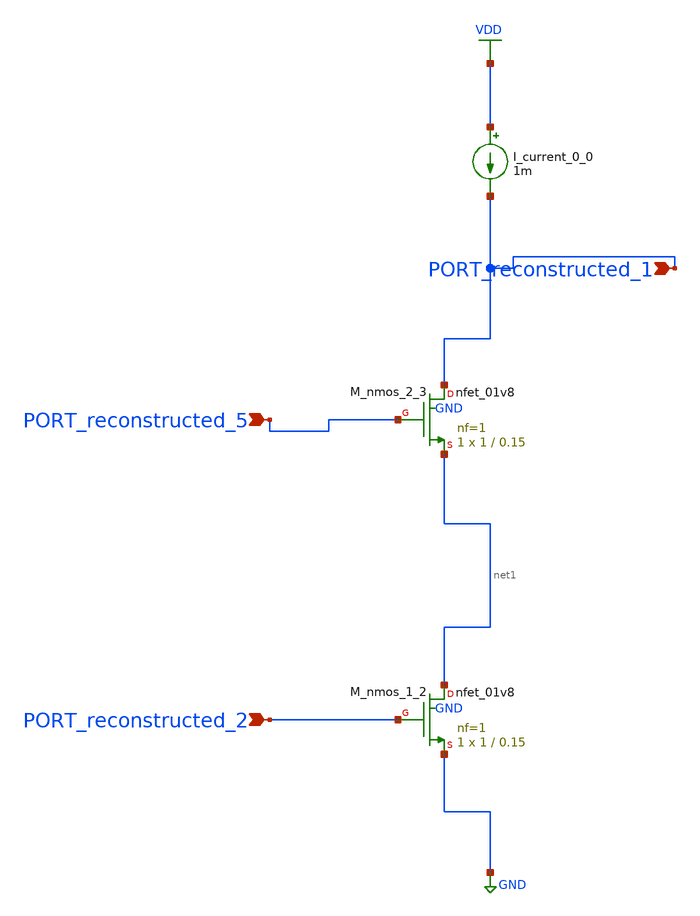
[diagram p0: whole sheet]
** sch_path: schematics/AMSNet/134.sch
**.subckt 134 PORT_reconstructed_5 PORT_reconstructed_2 PORT_reconstructed_1
*.ipin PORT_reconstructed_5
*.ipin PORT_reconstructed_2
*.ipin PORT_reconstructed_1
I_current_0_0 VDD PORT_reconstructed_1 1m
XM_nmos_1_2 net1 PORT_reconstructed_2 GND GND sky130_fd_pr__nfet_01v8 L=0.15 W=1 nf=1 ad='int((1 + 1)/2) * 1 / 1 * 0.29'
+ as='int((1 + 2)/2) * 1 / 1 * 0.29' pd='2*int((1 + 1)/2) * (1 / 1 + 0.29)' ps='2*int((1 + 2)/2) * (1 / 1 + 0.29)'
+ nrd='0.29 / 1 ' nrs='0.29 / 1 ' sa=0 sb=0 sd=0 mult=1 m=1
XM_nmos_2_3 PORT_reconstructed_1 PORT_reconstructed_5 net1 GND sky130_fd_pr__nfet_01v8 L=0.15 W=1 nf=1
+ ad='int((1 + 1)/2) * 1 / 1 * 0.29' as='int((1 + 2)/2) * 1 / 1 * 0.29' pd='2*int((1 + 1)/2) * (1 / 1 + 0.29)'
+ ps='2*int((1 + 2)/2) * (1 / 1 + 0.29)' nrd='0.29 / 1 ' nrs='0.29 / 1 ' sa=0 sb=0 sd=0 mult=1 m=1
**.ends
.GLOBAL GND
.GLOBAL VDD
.end
